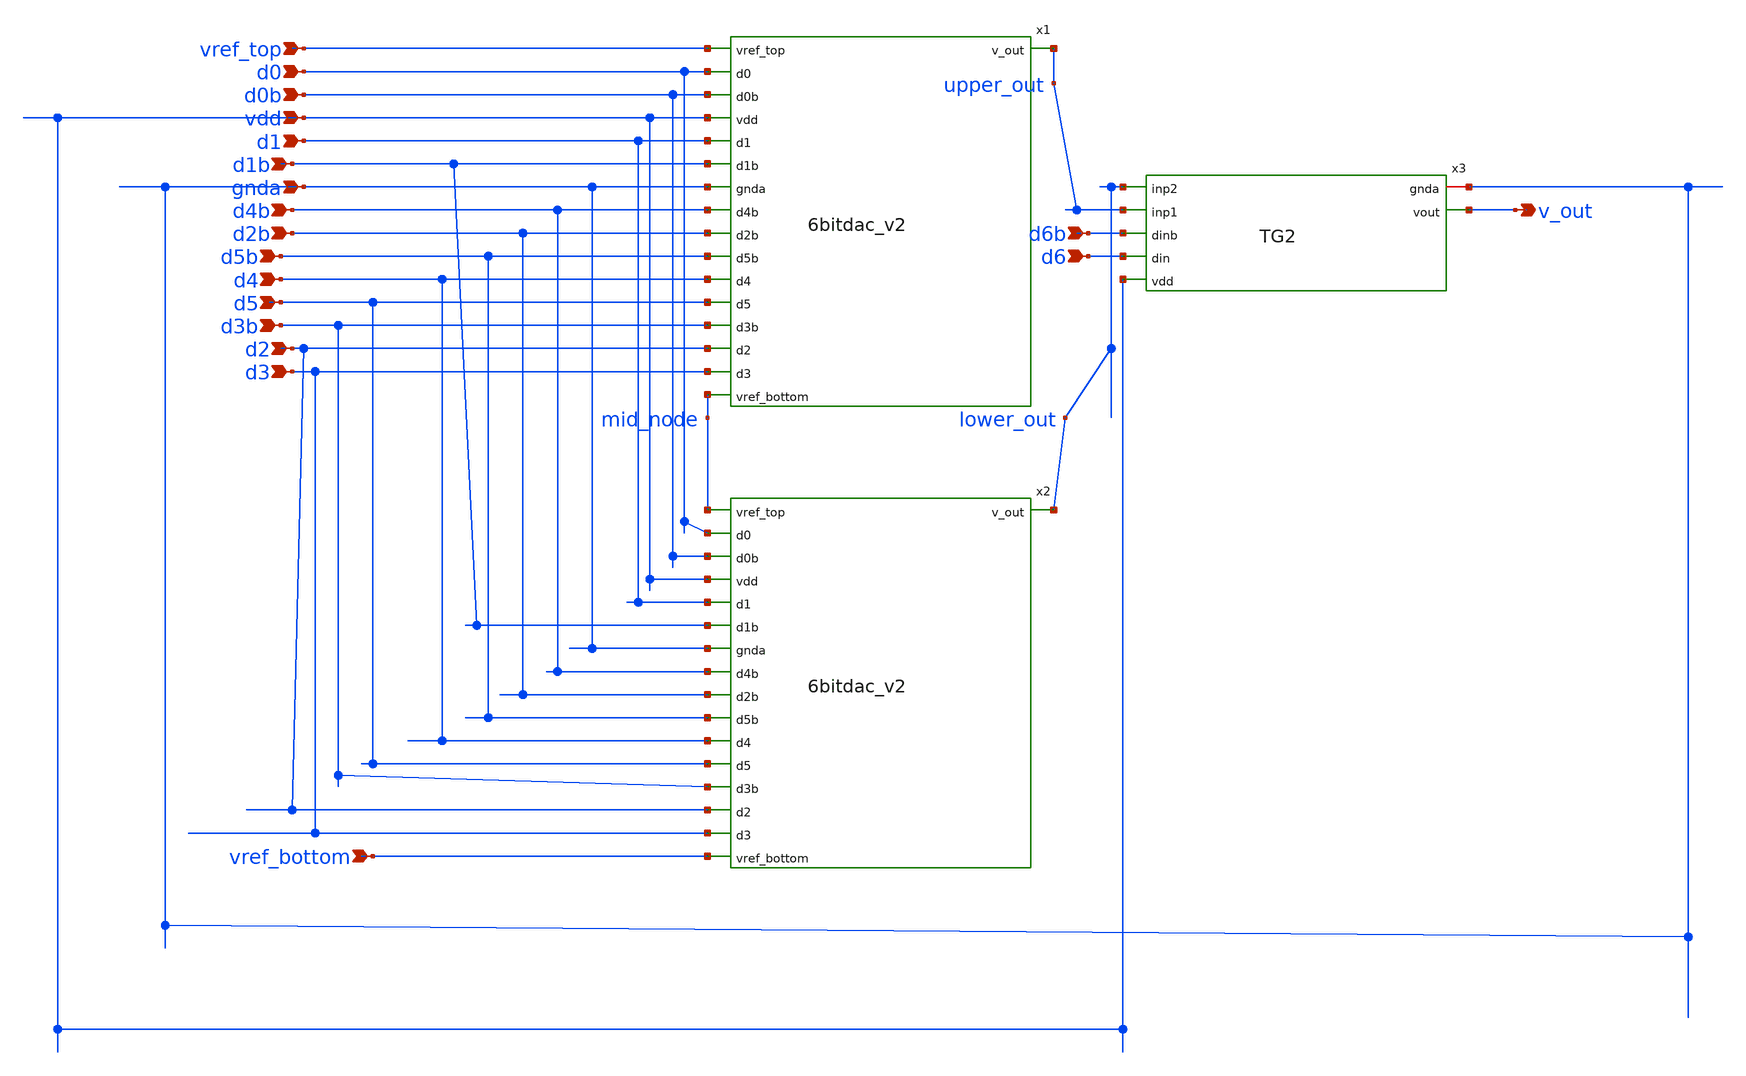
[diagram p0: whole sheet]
** sch_path: prelayout/7bitdac_v2.sch
**.subckt 7bitdac_v2 vref_top d0 d0b vdd d1 gnda d4b d2b d5b d4 d5 d3b d2 d3 d6b d6 v_out d1b
*+ vref_bottom
*.ipin vref_top
*.ipin d0
*.ipin d0b
*.ipin vdd
*.ipin d1
*.ipin gnda
*.ipin d4b
*.ipin d2b
*.ipin d5b
*.ipin d4
*.ipin d5
*.ipin d3b
*.ipin d2
*.ipin d3
*.ipin d6b
*.ipin d6
*.opin v_out
*.ipin d1b
*.ipin vref_bottom
x1 vref_top d0 d0b vdd d1 d1b gnda d4b upper_out d2b d5b d4 d5 d3b d2 d3 mid_node 6bitdac_v2
x2 mid_node d0 d0b vdd d1 d1b gnda d4b lower_out d2b d5b d4 d5 d3b d2 d3 vref_bottom 6bitdac_v2
Xx3 gnda v_out lower_out upper_out d6b d6 vdd TG2
**.ends
.end
